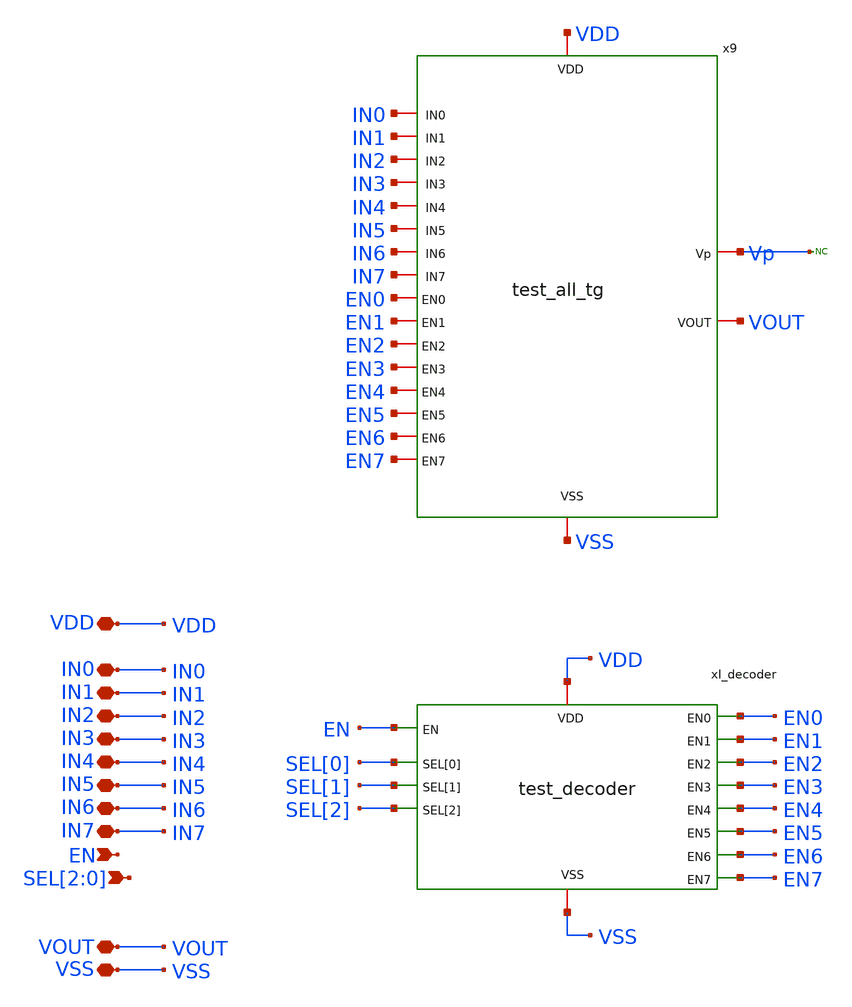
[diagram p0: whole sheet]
** sch_path: designs/libs/core_test/test_v2/test_v2.sch
**.subckt test_v2 VDD VSS VOUT EN SEL[2],SEL[1],SEL[0] IN0 IN1 IN2 IN3 IN4 IN5 IN6 IN7
*.iopin VDD
*.iopin VSS
*.iopin VOUT
*.ipin EN
*.ipin SEL[2],SEL[1],SEL[0]
*.iopin IN0
*.iopin IN1
*.iopin IN2
*.iopin IN3
*.iopin IN4
*.iopin IN5
*.iopin IN6
*.iopin IN7
xI_decoder SEL[0] SEL[1] SEL[2] VDD VSS EN0 EN1 EN2 EN3 EN4 EN5 EN6 EN7 EN test_decoder
* noconn Vp
x9 VDD VSS Vp VOUT IN0 IN1 IN2 IN3 IN4 IN5 IN6 IN7 EN0 EN1 EN2 EN3 EN4 EN5 EN6 EN7 test_all_tg
**.ends
.end
